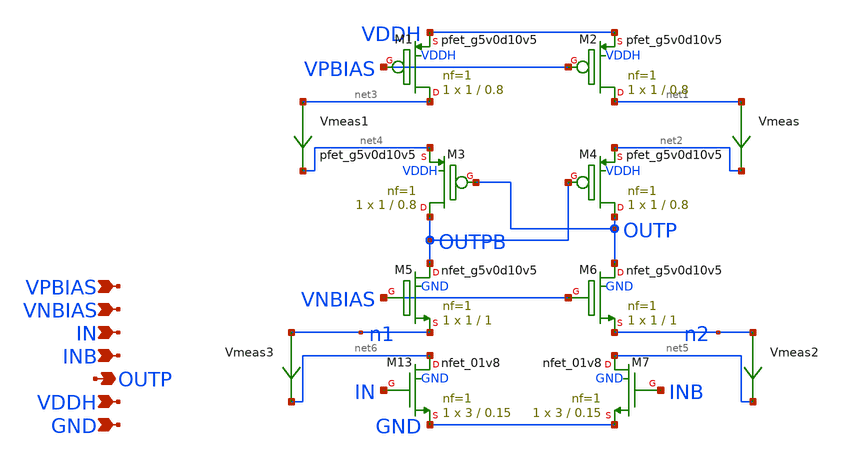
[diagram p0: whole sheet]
** sch_path: xschem/lvsf.sch
**.subckt lvsf IN INB OUTP VDDH GND VPBIAS VNBIAS
*.ipin IN
*.ipin INB
*.opin OUTP
*.ipin VDDH
*.ipin GND
*.ipin VPBIAS
*.ipin VNBIAS
Vmeas net1 net2 0
.save i(vmeas)
XM13 net6 IN GND GND sky130_fd_pr__nfet_01v8 L=0.15 W=3 nf=1 ad='int((nf+1)/2) * W/nf * 0.29' as='int((nf+2)/2) * W/nf * 0.29'
+ pd='2*int((nf+1)/2) * (W/nf + 0.29)' ps='2*int((nf+2)/2) * (W/nf + 0.29)' nrd='0.29 / W' nrs='0.29 / W'
+ sa=0 sb=0 sd=0 mult=1 m=1
XM1 net3 VPBIAS VDDH VDDH sky130_fd_pr__pfet_g5v0d10v5 L=0.8 W=1 nf=1 ad='int((nf+1)/2) * W/nf * 0.29'
+ as='int((nf+2)/2) * W/nf * 0.29' pd='2*int((nf+1)/2) * (W/nf + 0.29)' ps='2*int((nf+2)/2) * (W/nf + 0.29)'
+ nrd='0.29 / W' nrs='0.29 / W' sa=0 sb=0 sd=0 mult=1 m=1
XM2 net1 VPBIAS VDDH VDDH sky130_fd_pr__pfet_g5v0d10v5 L=0.8 W=1 nf=1 ad='int((nf+1)/2) * W/nf * 0.29'
+ as='int((nf+2)/2) * W/nf * 0.29' pd='2*int((nf+1)/2) * (W/nf + 0.29)' ps='2*int((nf+2)/2) * (W/nf + 0.29)'
+ nrd='0.29 / W' nrs='0.29 / W' sa=0 sb=0 sd=0 mult=1 m=1
XM3 OUTPB OUTP net4 VDDH sky130_fd_pr__pfet_g5v0d10v5 L=0.8 W=1 nf=1 ad='int((nf+1)/2) * W/nf * 0.29'
+ as='int((nf+2)/2) * W/nf * 0.29' pd='2*int((nf+1)/2) * (W/nf + 0.29)' ps='2*int((nf+2)/2) * (W/nf + 0.29)'
+ nrd='0.29 / W' nrs='0.29 / W' sa=0 sb=0 sd=0 mult=1 m=1
XM4 OUTP OUTPB net2 VDDH sky130_fd_pr__pfet_g5v0d10v5 L=0.8 W=1 nf=1 ad='int((nf+1)/2) * W/nf * 0.29'
+ as='int((nf+2)/2) * W/nf * 0.29' pd='2*int((nf+1)/2) * (W/nf + 0.29)' ps='2*int((nf+2)/2) * (W/nf + 0.29)'
+ nrd='0.29 / W' nrs='0.29 / W' sa=0 sb=0 sd=0 mult=1 m=1
XM5 OUTPB VNBIAS n1 GND sky130_fd_pr__nfet_g5v0d10v5 L=1 W=1 nf=1 ad='int((nf+1)/2) * W/nf * 0.29' as='int((nf+2)/2) * W/nf * 0.29'
+ pd='2*int((nf+1)/2) * (W/nf + 0.29)' ps='2*int((nf+2)/2) * (W/nf + 0.29)' nrd='0.29 / W' nrs='0.29 / W'
+ sa=0 sb=0 sd=0 mult=1 m=1
XM6 OUTP VNBIAS n2 GND sky130_fd_pr__nfet_g5v0d10v5 L=1 W=1 nf=1 ad='int((nf+1)/2) * W/nf * 0.29' as='int((nf+2)/2) * W/nf * 0.29'
+ pd='2*int((nf+1)/2) * (W/nf + 0.29)' ps='2*int((nf+2)/2) * (W/nf + 0.29)' nrd='0.29 / W' nrs='0.29 / W'
+ sa=0 sb=0 sd=0 mult=1 m=1
Vmeas1 net3 net4 0
.save i(vmeas1)
XM7 net5 INB GND GND sky130_fd_pr__nfet_01v8 L=0.15 W=3 nf=1 ad='int((nf+1)/2) * W/nf * 0.29' as='int((nf+2)/2) * W/nf * 0.29'
+ pd='2*int((nf+1)/2) * (W/nf + 0.29)' ps='2*int((nf+2)/2) * (W/nf + 0.29)' nrd='0.29 / W' nrs='0.29 / W'
+ sa=0 sb=0 sd=0 mult=1 m=1
Vmeas2 n2 net5 0
.save i(vmeas2)
Vmeas3 n1 net6 0
.save i(vmeas3)
**.ends
.end
